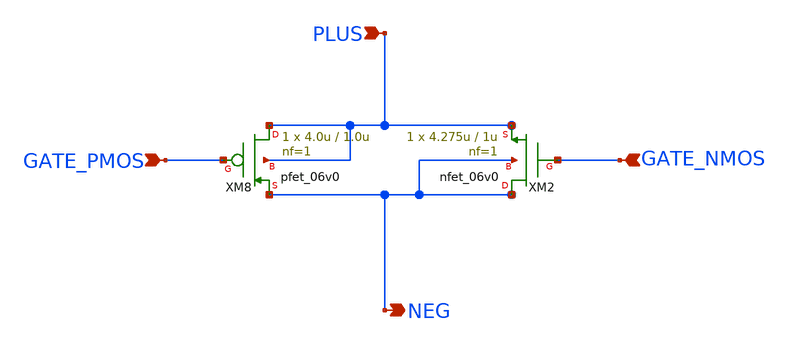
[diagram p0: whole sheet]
** sch_path: activities/opamp3AKAM/simulations_testbench/9k.sch
**.subckt 9k NEG PLUS GATE_PMOS GATE_NMOS
*.opin NEG
*.ipin PLUS
*.ipin GATE_PMOS
*.ipin GATE_NMOS
XM2 NEG GATE_NMOS PLUS NEG nfet_06v0 L=1u W=4.275u nf=1 ad='int((nf+1)/2) * W/nf * 0.18u' as='int((nf+2)/2) * W/nf * 0.18u'
+ pd='2*int((nf+1)/2) * (W/nf + 0.18u)' ps='2*int((nf+2)/2) * (W/nf + 0.18u)' nrd='0.18u / W' nrs='0.18u / W'
+ sa=0 sb=0 sd=0 m=1
XM8 PLUS GATE_PMOS NEG PLUS pfet_06v0 L=1.0u W=4.0u nf=1 ad='int((nf+1)/2) * W/nf * 0.18u' as='int((nf+2)/2) * W/nf * 0.18u'
+ pd='2*int((nf+1)/2) * (W/nf + 0.18u)' ps='2*int((nf+2)/2) * (W/nf + 0.18u)' nrd='0.18u / W' nrs='0.18u / W'
+ sa=0 sb=0 sd=0 m=1
**.ends
.end
